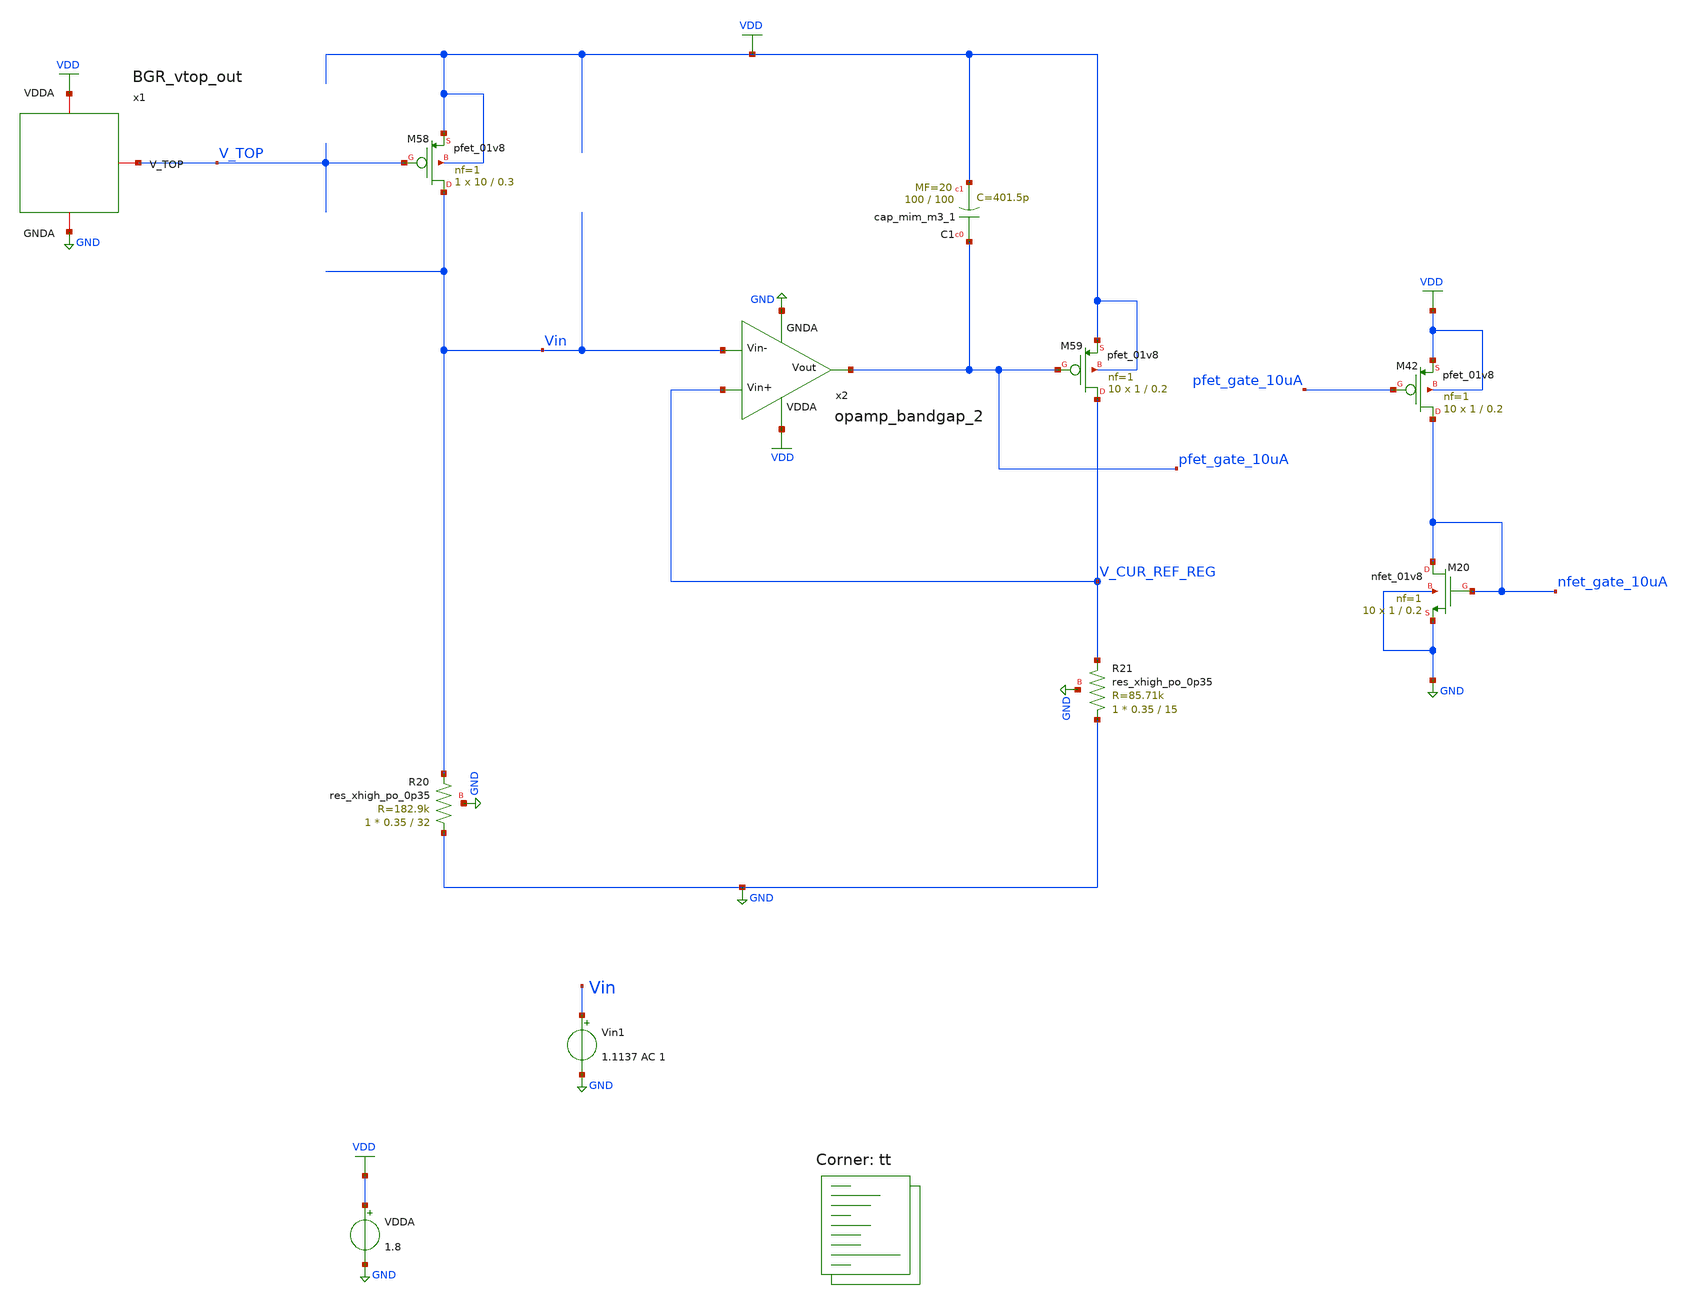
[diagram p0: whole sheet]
** sch_path: projects/opamp/xschem_ngspice/tb_BGR.sch
**.subckt tb_BGR
VDDA VDD GND 1.8
Vin1 Vin GND 1.1137 AC 1
XM42 nfet_gate_10uA pfet_gate_10uA VDD VDD sky130_fd_pr__pfet_01v8 L=0.2 W=1 nf=1 ad='int((nf+1)/2) * W/nf * 0.29'
+ as='int((nf+2)/2) * W/nf * 0.29' pd='2*int((nf+1)/2) * (W/nf + 0.29)' ps='2*int((nf+2)/2) * (W/nf + 0.29)'
+ nrd='0.29 / W' nrs='0.29 / W' sa=0 sb=0 sd=0 mult=10 m=10
XM58 Vin V_TOP VDD VDD sky130_fd_pr__pfet_01v8 L=0.3 W=10 nf=1 ad='int((nf+1)/2) * W/nf * 0.29' as='int((nf+2)/2) * W/nf * 0.29'
+ pd='2*int((nf+1)/2) * (W/nf + 0.29)' ps='2*int((nf+2)/2) * (W/nf + 0.29)' nrd='0.29 / W' nrs='0.29 / W'
+ sa=0 sb=0 sd=0 mult=1 m=1
XR20 GND Vin GND sky130_fd_pr__res_xhigh_po_0p35 L=32 mult=1 m=1
XR21 GND V_CUR_REF_REG GND sky130_fd_pr__res_xhigh_po_0p35 L=15 mult=1 m=1
XM59 V_CUR_REF_REG pfet_gate_10uA VDD VDD sky130_fd_pr__pfet_01v8 L=0.2 W=1 nf=1 ad='int((nf+1)/2) * W/nf * 0.29'
+ as='int((nf+2)/2) * W/nf * 0.29' pd='2*int((nf+1)/2) * (W/nf + 0.29)' ps='2*int((nf+2)/2) * (W/nf + 0.29)'
+ nrd='0.29 / W' nrs='0.29 / W' sa=0 sb=0 sd=0 mult=10 m=10
x1 V_TOP VDD GND BGR_vtop_out
x2 VDD pfet_gate_10uA Vin V_CUR_REF_REG GND opamp_bandgap_2
XM20 nfet_gate_10uA nfet_gate_10uA GND GND sky130_fd_pr__nfet_01v8 L=0.2 W=1 nf=1 ad='int((nf+1)/2) * W/nf * 0.29'
+ as='int((nf+2)/2) * W/nf * 0.29' pd='2*int((nf+1)/2) * (W/nf + 0.29)' ps='2*int((nf+2)/2) * (W/nf + 0.29)'
+ nrd='0.29 / W' nrs='0.29 / W' sa=0 sb=0 sd=0 mult=10 m=10
XC1 pfet_gate_10uA VDD sky130_fd_pr__cap_mim_m3_1 W=100 L=100 MF=20 m=20
**** begin user architecture code
.lib $::SKYWATER_MODELS/sky130.lib.spice tt




.option wnflag=1
.option savecurrents

* .param VDDGAUSS = agauss(1.8, 0.05, 1)
* .param VDD = VDDGAUSS
* .param VDD = 1.8

* .param TEMPGAUSS = agauss(40, 30, 1)
* .param temp = TEMPGAUSS
* .option temp = 26

.save @m.xm1.msky130_fd_pr__pfet_01v8[gm] @m.xm1.msky130_fd_pr__pfet_01v8[vds] @m.xm1.msky130_fd_pr__pfet_01v8[vth] @m.xm2.msky130_fd_pr__pfet_01v8[gm] @m.xm2.msky130_fd_pr__pfet_01v8[vds] @m.xm2.msky130_fd_pr__pfet_01v8[vth] @m.xm3.msky130_fd_pr__nfet_01v8[gm] @m.xm3.msky130_fd_pr__nfet_01v8[vds] @m.xm3.msky130_fd_pr__nfet_01v8[vth] @m.xm4.msky130_fd_pr__nfet_01v8[gm] @m.xm4.msky130_fd_pr__nfet_01v8[vds] @m.xm4.msky130_fd_pr__nfet_01v8[vth] @m.xm5.msky130_fd_pr__pfet_01v8[gm] @m.xm5.msky130_fd_pr__pfet_01v8[vds] @m.xm5.msky130_fd_pr__pfet_01v8[vth] @m.xm6.msky130_fd_pr__pfet_01v8[gm] @m.xm6.msky130_fd_pr__pfet_01v8[vds] @m.xm6.msky130_fd_pr__pfet_01v8[vth] @m.xm7.msky130_fd_pr__pfet_01v8[gm] @m.xm7.msky130_fd_pr__pfet_01v8[vds] @m.xm7.msky130_fd_pr__pfet_01v8[vth] @m.xm8.msky130_fd_pr__pfet_01v8[gm] @m.xm8.msky130_fd_pr__pfet_01v8[vds] @m.xm8.msky130_fd_pr__pfet_01v8[vth]

.control

  save all
  * tran 100p 1000n
  ac dec 20 1 1T
  write tb_BGR.raw
  set appendwrite
  show
.endc




**** end user architecture code
**.ends

* expanding   symbol:
*+  /foss/designs/my_design/projects/bandgapref/xschem_ngspice/new_files/BGR_vtop_out.sym # of pins=3
** sym_path: projects/bandgapref/xschem_ngspice/new_files/BGR_vtop_out.sym
** sch_path: projects/bandgapref/xschem_ngspice/new_files/BGR_vtop_out.sch
.subckt BGR_vtop_out V_TOP VDDA GNDA
*.iopin VDDA
*.iopin GNDA
*.opin V_TOP
XQ1 GNDA GNDA Vin- sky130_fd_pr__pnp_05v5_W3p40L3p40 m=1
XQ2 GNDA GNDA Vbe2 sky130_fd_pr__pnp_05v5_W3p40L3p40 m=8
XM1 Vin- V_TOP VDDA VDDA sky130_fd_pr__pfet_01v8 L=0.5 W=10 nf=1 ad='int((nf+1)/2) * W/nf * 0.29' as='int((nf+2)/2) * W/nf * 0.29'
+ pd='2*int((nf+1)/2) * (W/nf + 0.29)' ps='2*int((nf+2)/2) * (W/nf + 0.29)' nrd='0.29 / W' nrs='0.29 / W'
+ sa=0 sb=0 sd=0 mult=1 m=1
XM2 Vin+ V_TOP VDDA VDDA sky130_fd_pr__pfet_01v8 L=0.5 W=10 nf=1 ad='int((nf+1)/2) * W/nf * 0.29' as='int((nf+2)/2) * W/nf * 0.29'
+ pd='2*int((nf+1)/2) * (W/nf + 0.29)' ps='2*int((nf+2)/2) * (W/nf + 0.29)' nrd='0.29 / W' nrs='0.29 / W'
+ sa=0 sb=0 sd=0 mult=1 m=1
XR1 Vbe2 Vin+ GNDA sky130_fd_pr__res_xhigh_po_0p35 L=2.3 mult=1 m=1
XR2 GNDA Vin+ GNDA sky130_fd_pr__res_xhigh_po_0p35 L=18 mult=1 m=1
XR3 GNDA Vin- GNDA sky130_fd_pr__res_xhigh_po_0p35 L=18 mult=1 m=1
XM5 start_up start_up start_up_nfet1 start_up_nfet1 sky130_fd_pr__nfet_01v8 L=10 W=1 nf=1 ad='int((nf+1)/2) * W/nf * 0.29'
+ as='int((nf+2)/2) * W/nf * 0.29' pd='2*int((nf+1)/2) * (W/nf + 0.29)' ps='2*int((nf+2)/2) * (W/nf + 0.29)'
+ nrd='0.29 / W' nrs='0.29 / W' sa=0 sb=0 sd=0 mult=1 m=1
XM6 start_up V_TOP VDDA VDDA sky130_fd_pr__pfet_01v8 L=0.5 W=10 nf=1 ad='int((nf+1)/2) * W/nf * 0.29'
+ as='int((nf+2)/2) * W/nf * 0.29' pd='2*int((nf+1)/2) * (W/nf + 0.29)' ps='2*int((nf+2)/2) * (W/nf + 0.29)'
+ nrd='0.29 / W' nrs='0.29 / W' sa=0 sb=0 sd=0 mult=1 m=1
XM4 Vin- start_up V_TOP VDDA sky130_fd_pr__pfet_01v8 L=0.15 W=2 nf=1 ad='int((nf+1)/2) * W/nf * 0.29'
+ as='int((nf+2)/2) * W/nf * 0.29' pd='2*int((nf+1)/2) * (W/nf + 0.29)' ps='2*int((nf+2)/2) * (W/nf + 0.29)'
+ nrd='0.29 / W' nrs='0.29 / W' sa=0 sb=0 sd=0 mult=1 m=1
XM7 start_up_nfet1 start_up_nfet1 GNDA GNDA sky130_fd_pr__nfet_01v8 L=10 W=1 nf=1 ad='int((nf+1)/2) * W/nf * 0.29'
+ as='int((nf+2)/2) * W/nf * 0.29' pd='2*int((nf+1)/2) * (W/nf + 0.29)' ps='2*int((nf+2)/2) * (W/nf + 0.29)'
+ nrd='0.29 / W' nrs='0.29 / W' sa=0 sb=0 sd=0 mult=1 m=1
x1 VDDA V_TOP Vin- Vin+ GNDA opamp_bandgap_2
.ends


* expanding   symbol:
*+  /foss/designs/my_design/projects/bandgapref/xschem_ngspice/new_files/opamp_bandgap_2.sym # of pins=5
** sym_path: projects/bandgapref/xschem_ngspice/new_files/opamp_bandgap_2.sym
** sch_path: projects/bandgapref/xschem_ngspice/new_files/opamp_bandgap_2.sch
.subckt opamp_bandgap_2 VDDA Vout Vin- Vin+ GNDA
*.ipin Vin+
*.opin Vout
*.ipin Vin-
*.ipin GNDA
*.ipin VDDA
XM1 V_p VDDA GNDA GNDA sky130_fd_pr__nfet_01v8 L=5 W=2.5 nf=1 ad='int((nf+1)/2) * W/nf * 0.29' as='int((nf+2)/2) * W/nf * 0.29'
+ pd='2*int((nf+1)/2) * (W/nf + 0.29)' ps='2*int((nf+2)/2) * (W/nf + 0.29)' nrd='0.29 / W' nrs='0.29 / W'
+ sa=0 sb=0 sd=0 mult=1 m=1
XM2 V_mirror Vin- V_p GNDA sky130_fd_pr__nfet_01v8 L=0.2 W=2.5 nf=1 ad='int((nf+1)/2) * W/nf * 0.29'
+ as='int((nf+2)/2) * W/nf * 0.29' pd='2*int((nf+1)/2) * (W/nf + 0.29)' ps='2*int((nf+2)/2) * (W/nf + 0.29)'
+ nrd='0.29 / W' nrs='0.29 / W' sa=0 sb=0 sd=0 mult=1 m=1
XM3 1st_Vout Vin+ V_p GNDA sky130_fd_pr__nfet_01v8 L=0.2 W=2.5 nf=1 ad='int((nf+1)/2) * W/nf * 0.29'
+ as='int((nf+2)/2) * W/nf * 0.29' pd='2*int((nf+1)/2) * (W/nf + 0.29)' ps='2*int((nf+2)/2) * (W/nf + 0.29)'
+ nrd='0.29 / W' nrs='0.29 / W' sa=0 sb=0 sd=0 mult=1 m=1
XM5 V_mirror V_mirror VDDA VDDA sky130_fd_pr__pfet_01v8 L=0.2 W=6 nf=2 ad='int((nf+1)/2) * W/nf * 0.29'
+ as='int((nf+2)/2) * W/nf * 0.29' pd='2*int((nf+1)/2) * (W/nf + 0.29)' ps='2*int((nf+2)/2) * (W/nf + 0.29)'
+ nrd='0.29 / W' nrs='0.29 / W' sa=0 sb=0 sd=0 mult=1 m=1
XM6 1st_Vout V_mirror VDDA VDDA sky130_fd_pr__pfet_01v8 L=0.2 W=6 nf=2 ad='int((nf+1)/2) * W/nf * 0.29'
+ as='int((nf+2)/2) * W/nf * 0.29' pd='2*int((nf+1)/2) * (W/nf + 0.29)' ps='2*int((nf+2)/2) * (W/nf + 0.29)'
+ nrd='0.29 / W' nrs='0.29 / W' sa=0 sb=0 sd=0 mult=1 m=1
XM4 Vout VDDA GNDA GNDA sky130_fd_pr__nfet_01v8 L=5 W=2.5 nf=1 ad='int((nf+1)/2) * W/nf * 0.29' as='int((nf+2)/2) * W/nf * 0.29'
+ pd='2*int((nf+1)/2) * (W/nf + 0.29)' ps='2*int((nf+2)/2) * (W/nf + 0.29)' nrd='0.29 / W' nrs='0.29 / W'
+ sa=0 sb=0 sd=0 mult=1 m=1
XM7 Vout 1st_Vout VDDA VDDA sky130_fd_pr__pfet_01v8 L=0.2 W=6 nf=2 ad='int((nf+1)/2) * W/nf * 0.29' as='int((nf+2)/2) * W/nf * 0.29'
+ pd='2*int((nf+1)/2) * (W/nf + 0.29)' ps='2*int((nf+2)/2) * (W/nf + 0.29)' nrd='0.29 / W' nrs='0.29 / W'
+ sa=0 sb=0 sd=0 mult=1 m=1
XC1 1st_Vout net1 sky130_fd_pr__cap_mim_m3_1 W=10 L=10 MF=1 m=1
XR1 Vout net1 GNDA sky130_fd_pr__res_xhigh_po_0p35 L=0.5 mult=1 m=1
.ends

.GLOBAL GND
.GLOBAL VDD
.end
